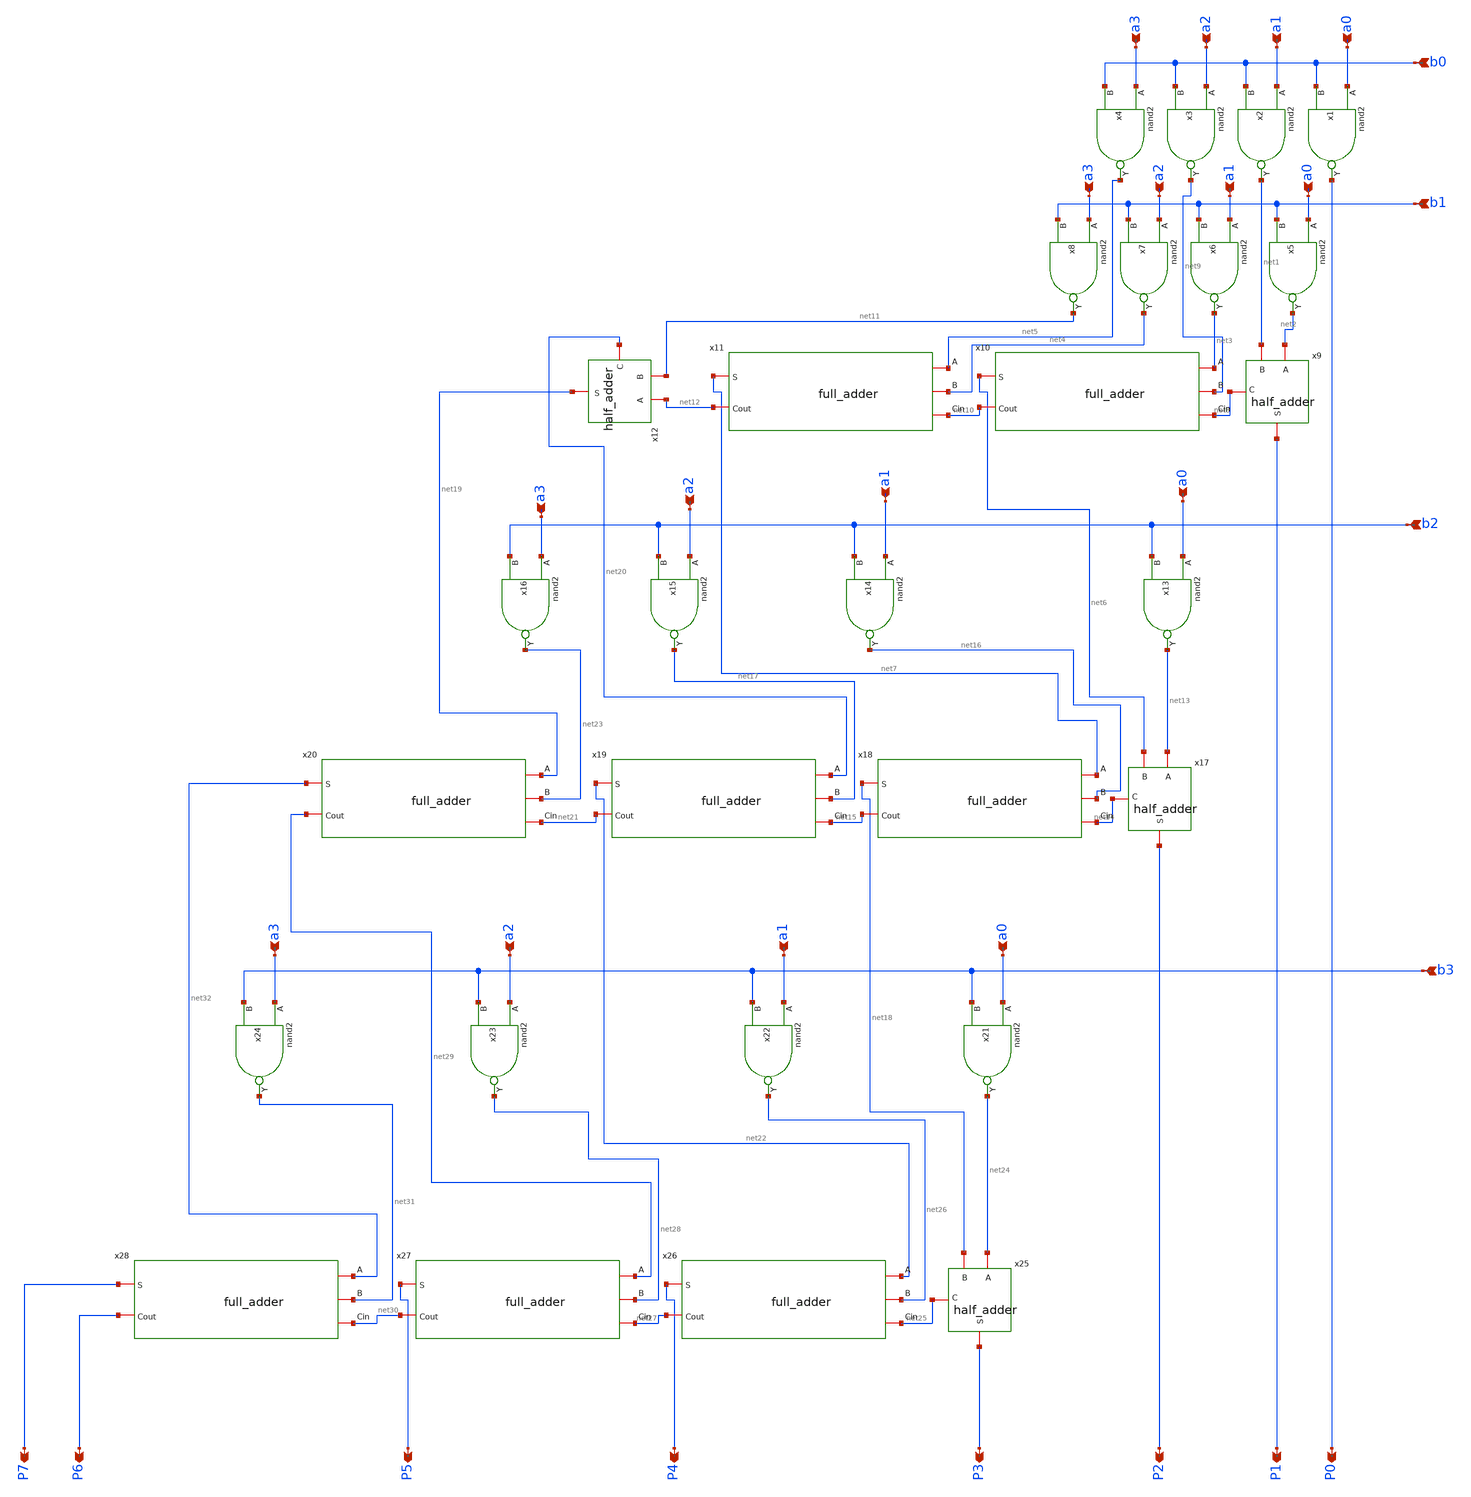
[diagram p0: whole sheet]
** sch_path: design/xschem/MULTIPLIER/multiplier.sch
**.subckt multiplier b0 b1 a3 a2 a1 a0 a0 a1 a2 a3 b2 b3 P3 P4 P5 P6 P7 P2 P0 a0 a1 a2 a3 a0 a1 a2
*+ a3 P1
*.ipin b0
*.ipin b1
*.ipin a3
*.ipin a2
*.ipin a1
*.ipin a0
*.ipin a0
*.ipin a1
*.ipin a2
*.ipin a3
*.ipin b2
*.ipin b3
*.opin P3
*.opin P4
*.opin P5
*.opin P6
*.opin P7
*.opin P2
*.opin P0
*.ipin a0
*.ipin a1
*.ipin a2
*.ipin a3
*.ipin a0
*.ipin a1
*.ipin a2
*.ipin a3
*.opin P1
x1 a0 b0 VSS VDD P0 nand2
x2 a1 b0 VSS VDD net1 nand2
x3 a2 b0 VSS VDD net9 nand2
x4 a3 b0 VSS VDD net5 nand2
x5 a0 b1 VSS VDD net2 nand2
x6 a1 b1 VSS VDD net3 nand2
x7 a2 b1 VSS VDD net4 nand2
x8 a3 b1 VSS VDD net11 nand2
x9 net2 P1 net1 net8 VSS VDD half_adder
x10 net3 net6 net9 net8 net10 full_adder
x11 net5 net7 net4 net10 net12 full_adder
x12 net12 net19 net11 net20 VSS VDD half_adder
x13 a0 b2 VSS VDD net13 nand2
x14 a1 b2 VSS VDD net16 nand2
x15 a2 b2 VSS VDD net17 nand2
x16 a3 b2 VSS VDD net23 nand2
x17 net13 P2 net6 net14 VSS VDD half_adder
x18 net7 net18 net16 net14 net15 full_adder
x19 net20 net22 net17 net15 net21 full_adder
x21 a0 b3 VSS VDD net24 nand2
x22 a1 b3 VSS VDD net26 nand2
x23 a2 b3 VSS VDD net28 nand2
x24 a3 b3 VSS VDD net31 nand2
x25 net24 P3 net18 net25 VSS VDD half_adder
x26 net22 P4 net26 net25 net27 full_adder
x27 net29 P5 net28 net27 net30 full_adder
x20 net19 net32 net23 net21 net29 full_adder
x28 net32 P7 net31 net30 P6 full_adder
**.ends
.end
